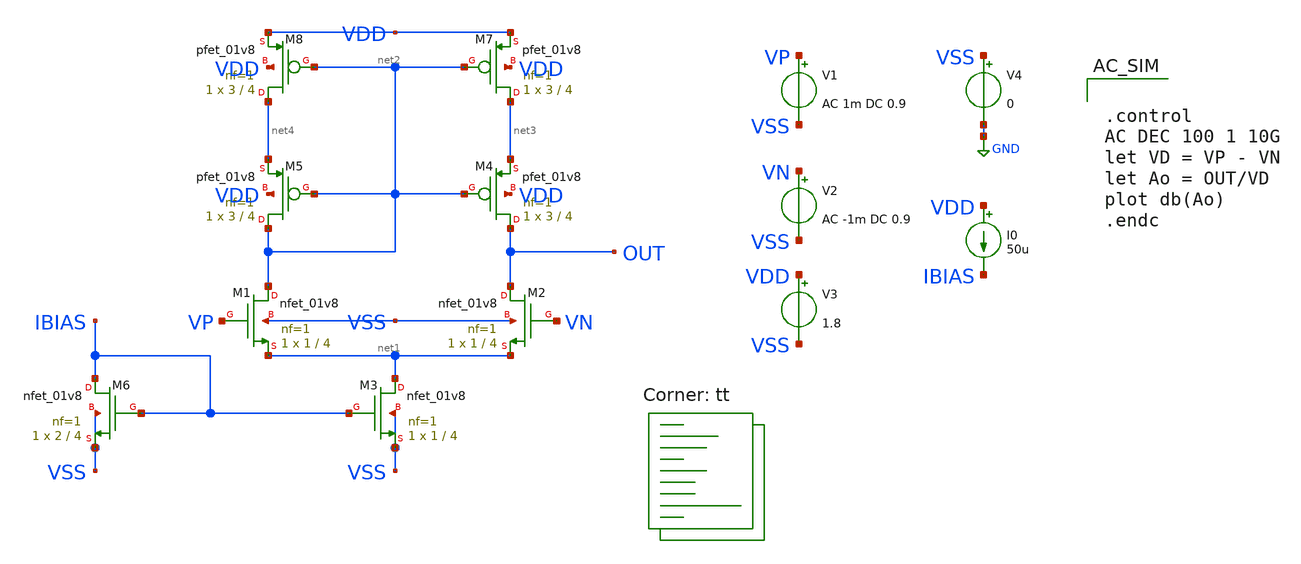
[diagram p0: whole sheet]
** sch_path: designs/libs/core_analog/core_bandgap/5t-ota/n-ota.sch
**.subckt n-ota
XM1 net2 VP net1 VSS sky130_fd_pr__nfet_01v8 L=4 W=1 nf=1 ad='int((nf+1)/2) * W/nf * 0.29' as='int((nf+2)/2) * W/nf * 0.29'
+ pd='2*int((nf+1)/2) * (W/nf + 0.29)' ps='2*int((nf+2)/2) * (W/nf + 0.29)' nrd='0.29 / W' nrs='0.29 / W'
+ sa=0 sb=0 sd=0 mult=1 m=1
XM2 OUT VN net1 VSS sky130_fd_pr__nfet_01v8 L=4 W=1 nf=1 ad='int((nf+1)/2) * W/nf * 0.29' as='int((nf+2)/2) * W/nf * 0.29'
+ pd='2*int((nf+1)/2) * (W/nf + 0.29)' ps='2*int((nf+2)/2) * (W/nf + 0.29)' nrd='0.29 / W' nrs='0.29 / W'
+ sa=0 sb=0 sd=0 mult=1 m=1
XM3 net1 IBIAS VSS VSS sky130_fd_pr__nfet_01v8 L=4 W=1 nf=1 ad='int((nf+1)/2) * W/nf * 0.29' as='int((nf+2)/2) * W/nf * 0.29'
+ pd='2*int((nf+1)/2) * (W/nf + 0.29)' ps='2*int((nf+2)/2) * (W/nf + 0.29)' nrd='0.29 / W' nrs='0.29 / W'
+ sa=0 sb=0 sd=0 mult=1 m=1
XM4 OUT net2 net3 VDD sky130_fd_pr__pfet_01v8 L=4 W=3 nf=1 ad='int((nf+1)/2) * W/nf * 0.29' as='int((nf+2)/2) * W/nf * 0.29'
+ pd='2*int((nf+1)/2) * (W/nf + 0.29)' ps='2*int((nf+2)/2) * (W/nf + 0.29)' nrd='0.29 / W' nrs='0.29 / W'
+ sa=0 sb=0 sd=0 mult=1 m=1
XM5 net2 net2 net4 VDD sky130_fd_pr__pfet_01v8 L=4 W=3 nf=1 ad='int((nf+1)/2) * W/nf * 0.29' as='int((nf+2)/2) * W/nf * 0.29'
+ pd='2*int((nf+1)/2) * (W/nf + 0.29)' ps='2*int((nf+2)/2) * (W/nf + 0.29)' nrd='0.29 / W' nrs='0.29 / W'
+ sa=0 sb=0 sd=0 mult=1 m=1
XM6 IBIAS IBIAS VSS VSS sky130_fd_pr__nfet_01v8 L=4 W=2 nf=1 ad='int((nf+1)/2) * W/nf * 0.29' as='int((nf+2)/2) * W/nf * 0.29'
+ pd='2*int((nf+1)/2) * (W/nf + 0.29)' ps='2*int((nf+2)/2) * (W/nf + 0.29)' nrd='0.29 / W' nrs='0.29 / W'
+ sa=0 sb=0 sd=0 mult=1 m=1
V1 VP VSS AC 1m DC 0.9
V2 VN VSS AC -1m DC 0.9
V3 VDD VSS 1.8
V4 VSS GND 0
I0 VDD IBIAS 50u
XM7 net3 net2 VDD VDD sky130_fd_pr__pfet_01v8 L=4 W=3 nf=1 ad='int((nf+1)/2) * W/nf * 0.29' as='int((nf+2)/2) * W/nf * 0.29'
+ pd='2*int((nf+1)/2) * (W/nf + 0.29)' ps='2*int((nf+2)/2) * (W/nf + 0.29)' nrd='0.29 / W' nrs='0.29 / W'
+ sa=0 sb=0 sd=0 mult=1 m=1
XM8 net4 net2 VDD VDD sky130_fd_pr__pfet_01v8 L=4 W=3 nf=1 ad='int((nf+1)/2) * W/nf * 0.29' as='int((nf+2)/2) * W/nf * 0.29'
+ pd='2*int((nf+1)/2) * (W/nf + 0.29)' ps='2*int((nf+2)/2) * (W/nf + 0.29)' nrd='0.29 / W' nrs='0.29 / W'
+ sa=0 sb=0 sd=0 mult=1 m=1
**** begin user architecture code
.lib $::SKYWATER_MODELS/sky130.lib.spice tt


.control
AC DEC 100 1 10G
let VD = VP - VN
let Ao = OUT/VD
plot db(Ao)
.endc


**** end user architecture code
**.ends
.GLOBAL GND
.end
